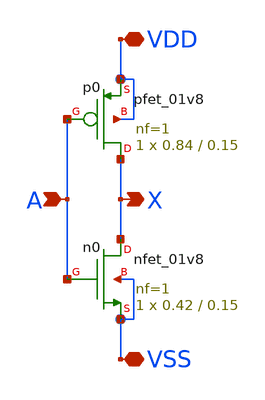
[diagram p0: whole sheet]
** sch_path: fullcustom/cad/inv/sch/inv.sch
* Copyright 2021 Stefan Frederik Schippers
* Licensed under the Apache License, Version 2.0 (the "License");
* you may not use this file except in compliance with the License.
* You may obtain a copy of the License at
* https://www.apache.org/licenses/LICENSE-2.0
* Unless required by applicable law or agreed to in writing, software
* distributed under the License is distributed on an "AS IS" BASIS,
* WITHOUT WARRANTIES OR CONDITIONS OF ANY KIND, either express or implied.
* See the License for the specific language governing permissions and
* limitations under the License.
**.subckt inv A VDD X VSS
*.ipin A
*.iopin VDD
*.opin X
*.iopin VSS
Xn0 X A VSS VSS sky130_fd_pr__nfet_01v8 L=0.15 W=0.42 nf=1 ad='int((1 + 1)/2) * 0.42 / 1 * 0.29' as='int((1 + 2)/2) * 0.42 / 1 * 0.29'
+ pd='2*int((1 + 1)/2) * (0.42 / 1 + 0.29)' ps='2*int((1 + 2)/2) * (0.42 / 1 + 0.29)' nrd='0.29 / 0.42 '
+ nrs='0.29 / 0.42 ' sa=0 sb=0 sd=0 mult=1 m=1
Xp0 X A VDD VDD sky130_fd_pr__pfet_01v8 L=0.15 W=0.84 nf=1 ad='int((nf+1)/2) * W/nf * 0.29' as='int((nf+2)/2) * W/nf * 0.29'
+ pd='2*int((nf+1)/2) * (W/nf + 0.29)' ps='2*int((nf+2)/2) * (W/nf + 0.29)' nrd='0.29 / W' nrs='0.29 / W'
+ sa=0 sb=0 sd=0 mult=1 m=1
**.ends
.end
